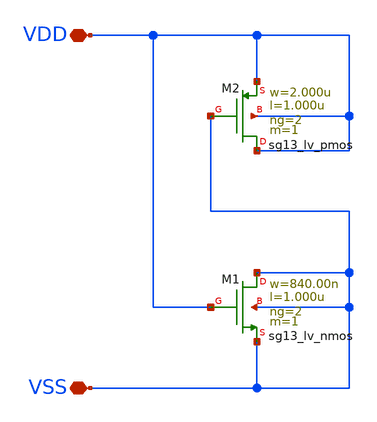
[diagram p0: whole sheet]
** sch_path: ihp-sg13g2/libs.tech/xschem/sg13g2_stdcells/sg13g2_decap_8.sch
**.subckt sg13g2_decap_8 VDD VSS
*.iopin VDD
*.iopin VSS
XM1 VSS VDD VSS VSS sg13_lv_nmos w=840.00n l=1.000u ng=2 m=1 mm_ok=1
XM2 VDD VSS VDD VDD sg13_lv_pmos w=2.000u l=1.000u ng=2 m=1 mm_ok=1
**.ends
.end
